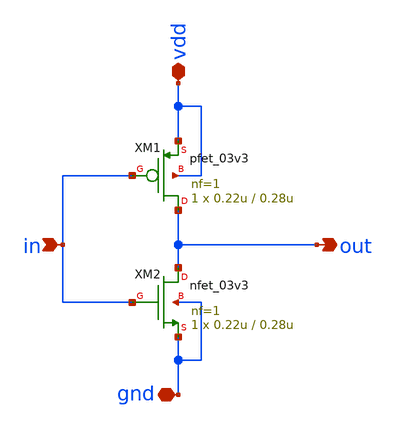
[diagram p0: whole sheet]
** sch_path: xschem/c2v_frontend/inverter.sch
**.subckt inverter vdd gnd in out
*.iopin vdd
*.iopin gnd
*.ipin in
*.opin out
XM1 out in vdd vdd pfet_03v3 L=0.28u W=0.22u nf=1 ad='int((nf+1)/2) * W/nf * 0.18u' as='int((nf+2)/2) * W/nf * 0.18u'
+ pd='2*int((nf+1)/2) * (W/nf + 0.18u)' ps='2*int((nf+2)/2) * (W/nf + 0.18u)' nrd='0.18u / W' nrs='0.18u / W'
+ sa=0 sb=0 sd=0 m=1
XM2 out in gnd gnd nfet_03v3 L=0.28u W=0.22u nf=1 ad='int((nf+1)/2) * W/nf * 0.18u' as='int((nf+2)/2) * W/nf * 0.18u'
+ pd='2*int((nf+1)/2) * (W/nf + 0.18u)' ps='2*int((nf+2)/2) * (W/nf + 0.18u)' nrd='0.18u / W' nrs='0.18u / W'
+ sa=0 sb=0 sd=0 m=1
**.ends
.end
